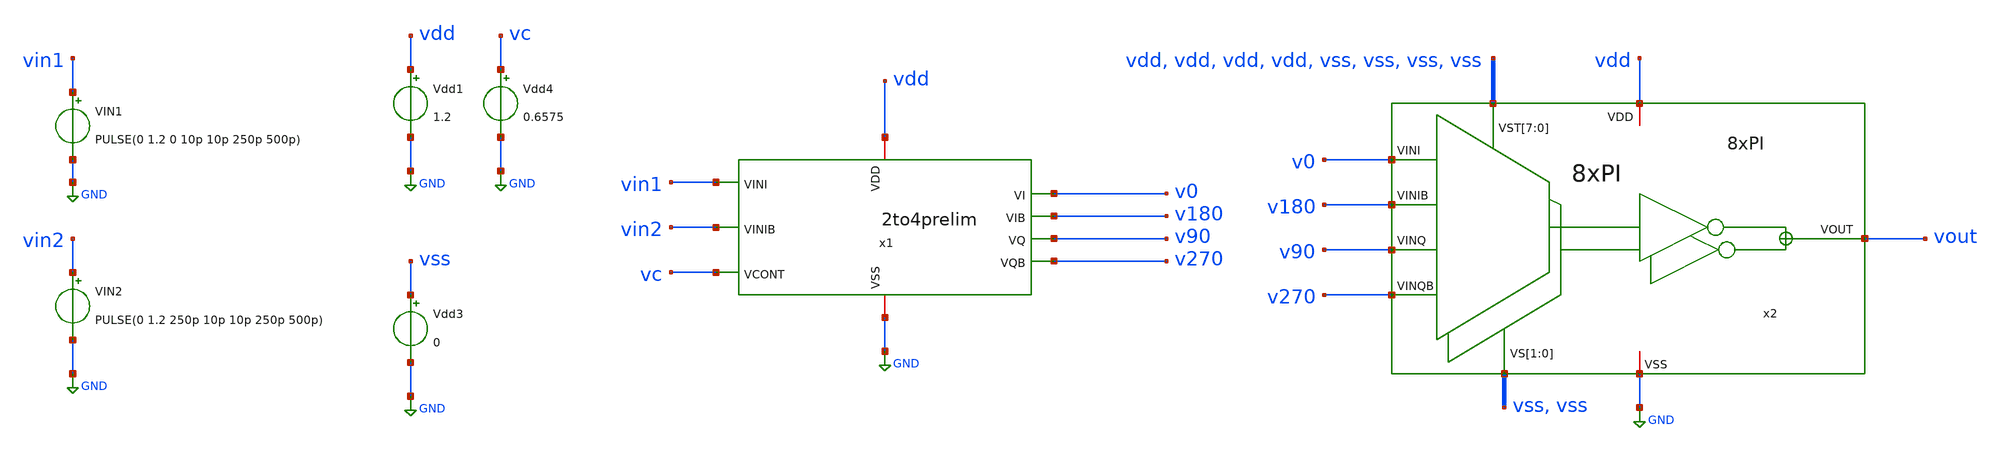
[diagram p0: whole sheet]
** sch_path: 2to4/tb_2to4prelim.sch
**.subckt tb_2to4prelim
Vdd1 vdd GND 1.2
VIN1 vin1 GND PULSE(0 1.2 0 10p 10p 250p 500p)
VIN2 vin2 GND PULSE(0 1.2 250p 10p 10p 250p 500p)
x1 vdd v270 v90 vin1 GND vc v180 v0 vin2 2to4prelim
Vdd4 vc GND 0.6575
x2 v0 v180 v90 v270 vss vss vdd vdd vdd vdd vss vss vss vss vout vdd GND 8xPI
Vdd3 vss GND 0
**** begin user architecture code


.save v(vin1) v(v0) v(v90) v(v270) v(v180) v(vin2) v(vout)

.tran 10p 3n
.save all

.control
run
set color0=white
write tran_logic.raw

* --- 1. MEDICIONES DE FASE Y RETARDO (Usando v90) ---
* Periodo Entrada (Ref)
meas tran T_per TRIG v(vin1) VAL=0.6 RISE=3 TARG v(vin1) VAL=0.6 RISE=4

* Retardo (Entrada vs v90)
meas tran T_del TRIG v(vin1) VAL=0.6 RISE=3 TARG v(v90) VAL=0.6 RISE=3

* Calculo Fase
let Phase_Deg = (T_del / T_per) * 360

print T_per
print T_del
print Phase_Deg


* --- 2. DUTY CYCLE (Usando v90) ---
* Periodo Salida
meas tran T_period TRIG v(v90) VAL=0.6 RISE=2 TARG v(v90) VAL=0.6 RISE=3

* Tiempo en ALTO (Ton)
* Desde que sube (RISE=2) hasta que baja (FALL=2)
meas tran T_high TRIG v(v90) VAL=0.6 RISE=2 TARG v(v90) VAL=0.6 FALL=2

* Tiempo en BAJO (Toff)
* Desde que baja (FALL=2) hasta que sube de nuevo (RISE=3)
meas tran T_low TRIG v(v90) VAL=0.6 FALL=2 TARG v(v90) VAL=0.6 RISE=3

let Duty_High = (T_high / T_period) * 100
let Duty_Low  = (T_low / T_period) * 100

print Duty_High
print Duty_Low
.endc



.lib cornerMOSlv.lib mos_tt
.include /foss/pdks/ihp-sg13g2/libs.ref/sg13g2_stdcell/spice/sg13g2_stdcell.spice


**** end user architecture code
**.ends
.GLOBAL GND
.end
